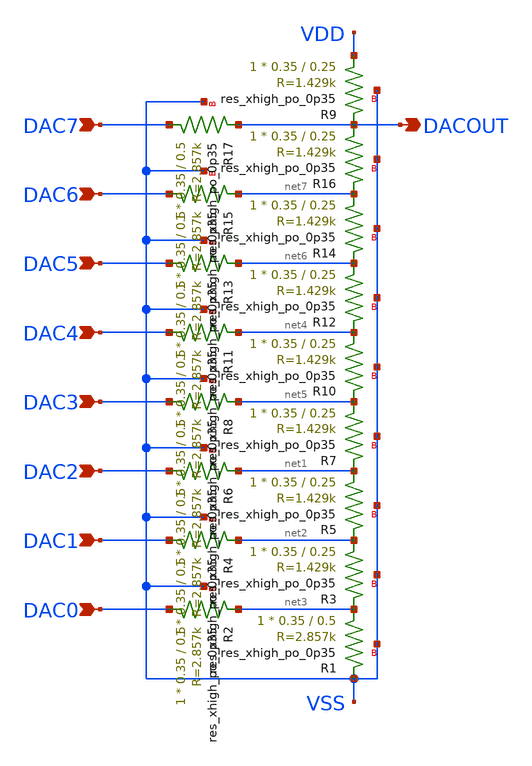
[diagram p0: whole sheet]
** sch_path: archive/tt_um_wulf_8bit_vco/xschem/lib/dac_8bit.sch
**.subckt dac_8bit DAC3 DAC2 DAC1 DAC0 DACOUT DAC4 DAC5 DAC6 DAC7
*.ipin DAC3
*.ipin DAC2
*.ipin DAC1
*.ipin DAC0
*.opin DACOUT
*.ipin DAC4
*.ipin DAC5
*.ipin DAC6
*.ipin DAC7
XR1 net3 VSS VSS sky130_fd_pr__res_xhigh_po_0p35 L=0.5 mult=1 m=1
XR2 DAC0 net3 VSS sky130_fd_pr__res_xhigh_po_0p35 L=0.5 mult=1 m=1
XR3 net2 net3 VSS sky130_fd_pr__res_xhigh_po_0p35 L=0.25 mult=1 m=1
XR4 DAC1 net2 VSS sky130_fd_pr__res_xhigh_po_0p35 L=0.5 mult=1 m=1
XR5 net1 net2 VSS sky130_fd_pr__res_xhigh_po_0p35 L=0.25 mult=1 m=1
XR6 DAC2 net1 VSS sky130_fd_pr__res_xhigh_po_0p35 L=0.5 mult=1 m=1
XR7 net5 net1 VSS sky130_fd_pr__res_xhigh_po_0p35 L=0.25 mult=1 m=1
XR8 DAC3 net5 VSS sky130_fd_pr__res_xhigh_po_0p35 L=0.5 mult=1 m=1
XR9 VDD DACOUT VSS sky130_fd_pr__res_xhigh_po_0p35 L=0.25 mult=1 m=1
XR10 net4 net5 VSS sky130_fd_pr__res_xhigh_po_0p35 L=0.25 mult=1 m=1
XR11 DAC4 net4 VSS sky130_fd_pr__res_xhigh_po_0p35 L=0.5 mult=1 m=1
XR12 net6 net4 VSS sky130_fd_pr__res_xhigh_po_0p35 L=0.25 mult=1 m=1
XR13 DAC5 net6 VSS sky130_fd_pr__res_xhigh_po_0p35 L=0.5 mult=1 m=1
XR14 net7 net6 VSS sky130_fd_pr__res_xhigh_po_0p35 L=0.25 mult=1 m=1
XR15 DAC6 net7 VSS sky130_fd_pr__res_xhigh_po_0p35 L=0.5 mult=1 m=1
XR16 DACOUT net7 VSS sky130_fd_pr__res_xhigh_po_0p35 L=0.25 mult=1 m=1
XR17 DAC7 DACOUT VSS sky130_fd_pr__res_xhigh_po_0p35 L=0.5 mult=1 m=1
**.ends
.end
